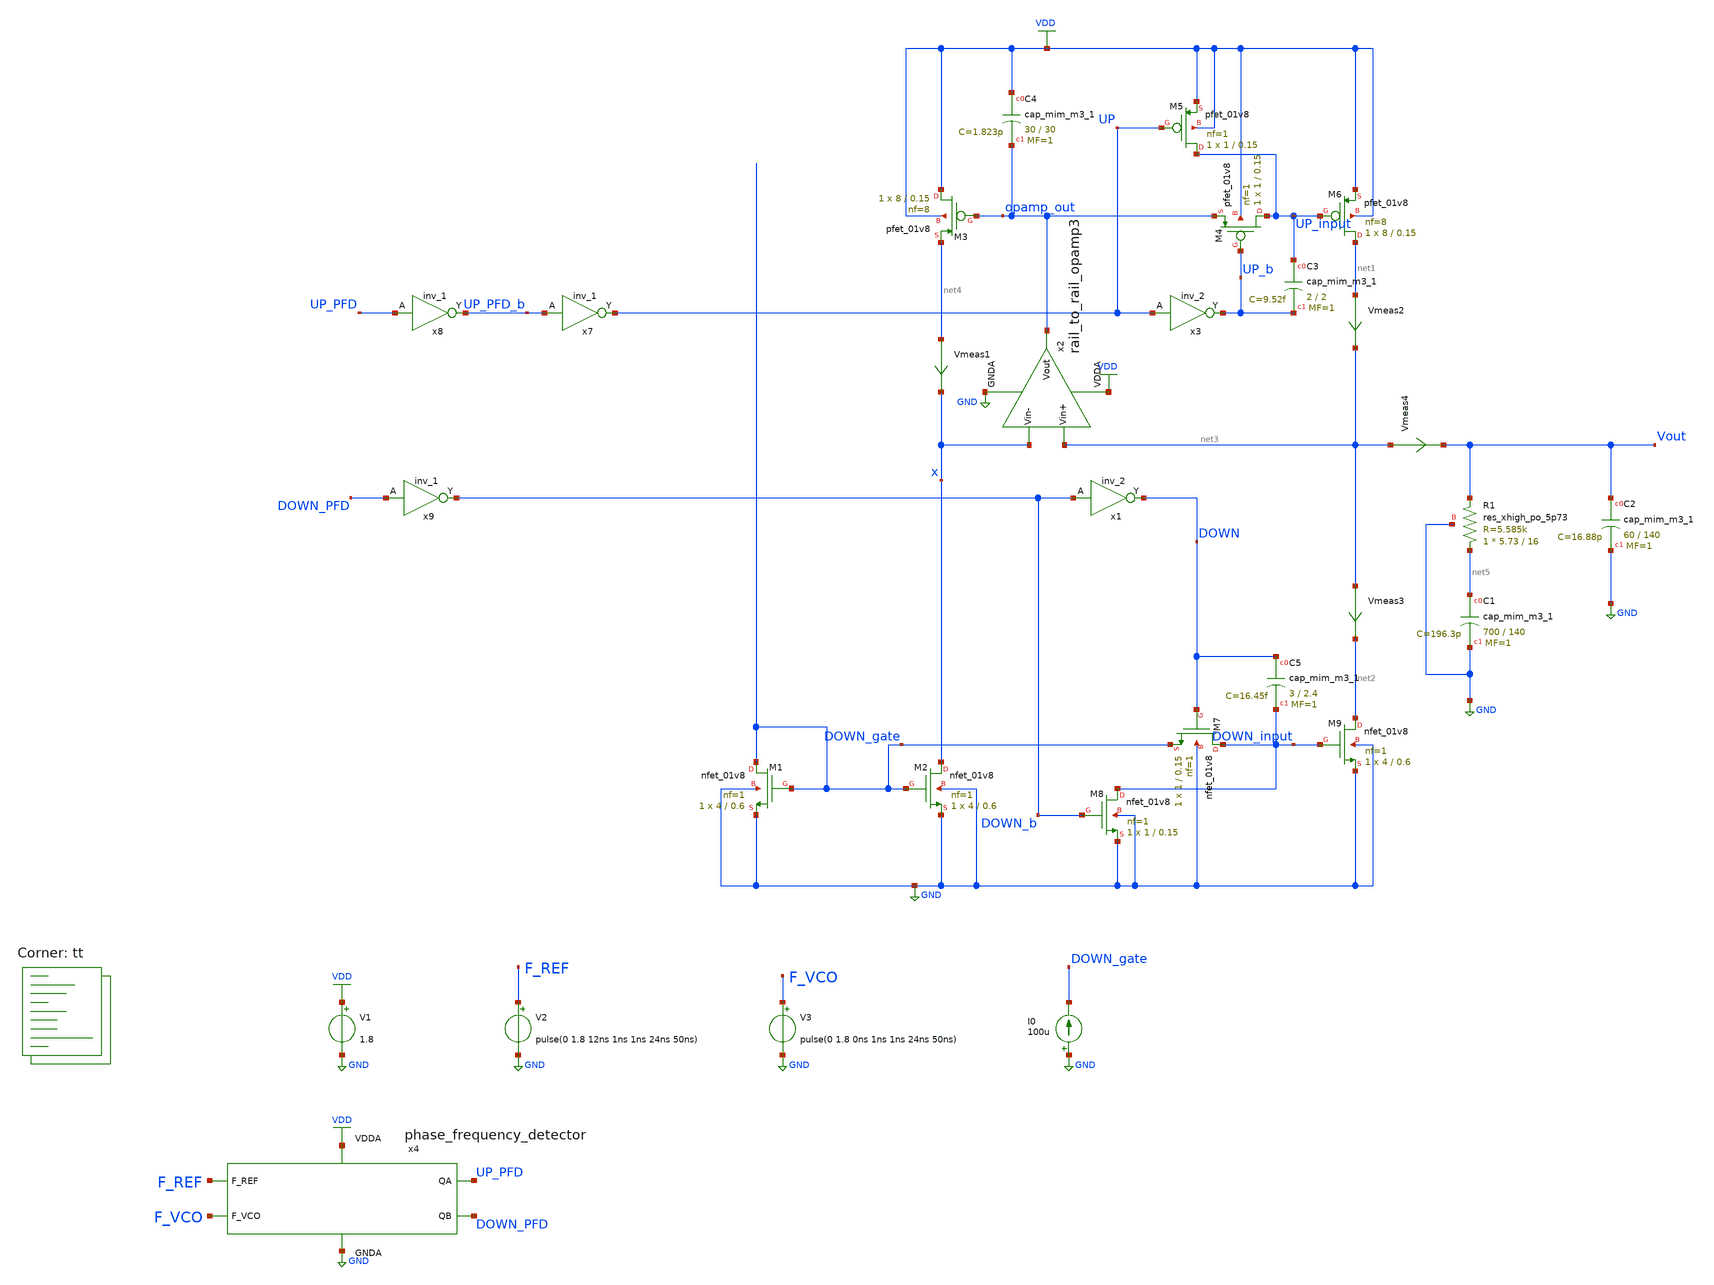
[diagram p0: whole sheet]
** sch_path: projects/pll/charge_pump/xschem_ngspice/pfd_charge_pump_dead_zone_check.sch
**.subckt pfd_charge_pump_dead_zone_check
XM1 DOWN_gate DOWN_gate GND GND sky130_fd_pr__nfet_01v8 L=0.6 W=4 nf=1 ad='int((nf+1)/2) * W/nf * 0.29'
+ as='int((nf+2)/2) * W/nf * 0.29' pd='2*int((nf+1)/2) * (W/nf + 0.29)' ps='2*int((nf+2)/2) * (W/nf + 0.29)'
+ nrd='0.29 / W' nrs='0.29 / W' sa=0 sb=0 sd=0 mult=1 m=1
XM2 x DOWN_gate GND GND sky130_fd_pr__nfet_01v8 L=0.6 W=4 nf=1 ad='int((nf+1)/2) * W/nf * 0.29' as='int((nf+2)/2) * W/nf * 0.29'
+ pd='2*int((nf+1)/2) * (W/nf + 0.29)' ps='2*int((nf+2)/2) * (W/nf + 0.29)' nrd='0.29 / W' nrs='0.29 / W'
+ sa=0 sb=0 sd=0 mult=1 m=1
XM3 VDD opamp_out net4 VDD sky130_fd_pr__pfet_01v8 L=0.15 W=8 nf=8 ad='int((nf+1)/2) * W/nf * 0.29' as='int((nf+2)/2) * W/nf * 0.29'
+ pd='2*int((nf+1)/2) * (W/nf + 0.29)' ps='2*int((nf+2)/2) * (W/nf + 0.29)' nrd='0.29 / W' nrs='0.29 / W'
+ sa=0 sb=0 sd=0 mult=1 m=1
V1 VDD GND 1.8
I0 GND DOWN_gate 100u
Vmeas1 net4 x 0
.save i(vmeas1)
XM4 UP_input UP_b opamp_out VDD sky130_fd_pr__pfet_01v8 L=0.15 W=1 nf=1 ad='int((nf+1)/2) * W/nf * 0.29'
+ as='int((nf+2)/2) * W/nf * 0.29' pd='2*int((nf+1)/2) * (W/nf + 0.29)' ps='2*int((nf+2)/2) * (W/nf + 0.29)'
+ nrd='0.29 / W' nrs='0.29 / W' sa=0 sb=0 sd=0 mult=1 m=1
XM5 UP_input UP VDD VDD sky130_fd_pr__pfet_01v8 L=0.15 W=1 nf=1 ad='int((nf+1)/2) * W/nf * 0.29' as='int((nf+2)/2) * W/nf * 0.29'
+ pd='2*int((nf+1)/2) * (W/nf + 0.29)' ps='2*int((nf+2)/2) * (W/nf + 0.29)' nrd='0.29 / W' nrs='0.29 / W'
+ sa=0 sb=0 sd=0 mult=1 m=1
XM6 net1 UP_input VDD VDD sky130_fd_pr__pfet_01v8 L=0.15 W=8 nf=8 ad='int((nf+1)/2) * W/nf * 0.29' as='int((nf+2)/2) * W/nf * 0.29'
+ pd='2*int((nf+1)/2) * (W/nf + 0.29)' ps='2*int((nf+2)/2) * (W/nf + 0.29)' nrd='0.29 / W' nrs='0.29 / W'
+ sa=0 sb=0 sd=0 mult=1 m=1
Vmeas2 net1 net3 0
.save i(vmeas2)
XM7 DOWN_input DOWN DOWN_gate GND sky130_fd_pr__nfet_01v8 L=0.15 W=1 nf=1 ad='int((nf+1)/2) * W/nf * 0.29'
+ as='int((nf+2)/2) * W/nf * 0.29' pd='2*int((nf+1)/2) * (W/nf + 0.29)' ps='2*int((nf+2)/2) * (W/nf + 0.29)'
+ nrd='0.29 / W' nrs='0.29 / W' sa=0 sb=0 sd=0 mult=1 m=1
XM8 DOWN_input DOWN_b GND GND sky130_fd_pr__nfet_01v8 L=0.15 W=1 nf=1 ad='int((nf+1)/2) * W/nf * 0.29'
+ as='int((nf+2)/2) * W/nf * 0.29' pd='2*int((nf+1)/2) * (W/nf + 0.29)' ps='2*int((nf+2)/2) * (W/nf + 0.29)'
+ nrd='0.29 / W' nrs='0.29 / W' sa=0 sb=0 sd=0 mult=1 m=1
Vmeas3 net3 net2 0
.save i(vmeas3)
XM9 net2 DOWN_input GND GND sky130_fd_pr__nfet_01v8 L=0.6 W=4 nf=1 ad='int((nf+1)/2) * W/nf * 0.29' as='int((nf+2)/2) * W/nf * 0.29'
+ pd='2*int((nf+1)/2) * (W/nf + 0.29)' ps='2*int((nf+2)/2) * (W/nf + 0.29)' nrd='0.29 / W' nrs='0.29 / W'
+ sa=0 sb=0 sd=0 mult=1 m=1
x7 UP_PFD_b GND GND VDD VDD UP sky130_fd_sc_hd__inv_1
x8 UP_PFD GND GND VDD VDD UP_PFD_b sky130_fd_sc_hd__inv_1
x9 DOWN_PFD GND GND VDD VDD DOWN_b sky130_fd_sc_hd__inv_1
x3 UP GND GND VDD VDD UP_b sky130_fd_sc_hd__inv_2
x1 DOWN_b GND GND VDD VDD DOWN sky130_fd_sc_hd__inv_2
XC2 Vout GND sky130_fd_pr__cap_mim_m3_1 W=60 L=140 MF=1 m=1
XC1 net5 GND sky130_fd_pr__cap_mim_m3_1 W=700 L=140 MF=1 m=1
V2 F_REF GND pulse(0 1.8 12ns 1ns 1ns 24ns 50ns)
V3 F_VCO GND pulse(0 1.8 0ns 1ns 1ns 24ns 50ns)
x4 F_REF F_VCO VDD UP_PFD DOWN_PFD GND phase_frequency_detector
Vmeas4 net3 Vout 0
.save i(vmeas4)
x2 VDD net3 x opamp_out GND rail_to_rail_opamp3
XC4 VDD opamp_out sky130_fd_pr__cap_mim_m3_1 W=30 L=30 MF=1 m=1
XC3 UP_input UP_b sky130_fd_pr__cap_mim_m3_1 W=2 L=2 MF=1 m=1
XC5 DOWN DOWN_input sky130_fd_pr__cap_mim_m3_1 W=3 L=2.4 MF=1 m=1
XR1 net5 Vout GND sky130_fd_pr__res_xhigh_po_5p73 L=16 mult=1 m=1
**** begin user architecture code
.lib $::SKYWATER_MODELS/sky130.lib.spice tt



.include /foss/pdks/sky130A/libs.ref/sky130_fd_sc_hd/spice/sky130_fd_sc_hd.spice

.option method=gear
.option wnflag=1

.ic v(vout) = 0.9

.control
  let start_delay = 0ns
  let stop_delay = 24ns
  let index = -12
  dowhile start_delay <= stop_delay

    alter @V3[pulse] = [ 0 1.8 $&start_delay 1ns 1ns 24ns 50ns ]
    save i(vmeas4#branch) v(F_REF) v(F_VCO) v(vout)
    tran 5ps 1us
    remzerovec
    linearize i(vmeas4) v(F_REF) v(F_VCO) v(vout)
    echo $&start_delay
    write pfd_charge_pump_dead_zone_check_1_{$&index}.raw
    wrdata /foss/designs/my_design/projects/pll/charge_pump/xschem_ngspice/pfd_charge_pump_dead_zone_check_1_{$&index}.txt
+ i(vmeas4)
    set appendwrite
    reset
    let index = index + 1
    let start_delay = start_delay + 1ns

  end
.endc




**** end user architecture code
**.ends
.GLOBAL VDD
.GLOBAL GND
.end
